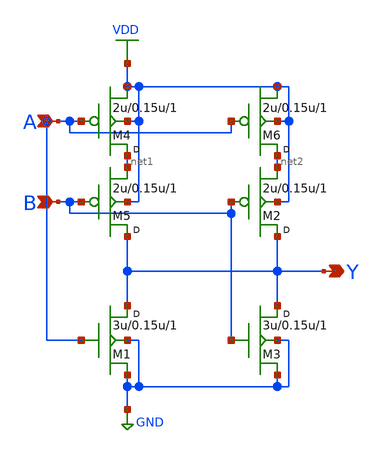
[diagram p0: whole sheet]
** sch_path: lib/xschem/schematics/NOR2X2.sch
**.subckt NOR2X2 Y B A
*.opin Y
*.ipin B
*.ipin A
M1 Y A GND GND nmos w=3u l=0.15u m=1
M3 Y B GND GND nmos w=3u l=0.15u m=1
M4 net1 A VDD VDD pmos w=2u l=0.15u m=1
M5 Y B net1 VDD pmos w=2u l=0.15u m=1
M2 Y B net2 VDD pmos w=2u l=0.15u m=1
M6 net2 A VDD VDD pmos w=2u l=0.15u m=1
**.ends
.GLOBAL GND
.GLOBAL VDD
.end
